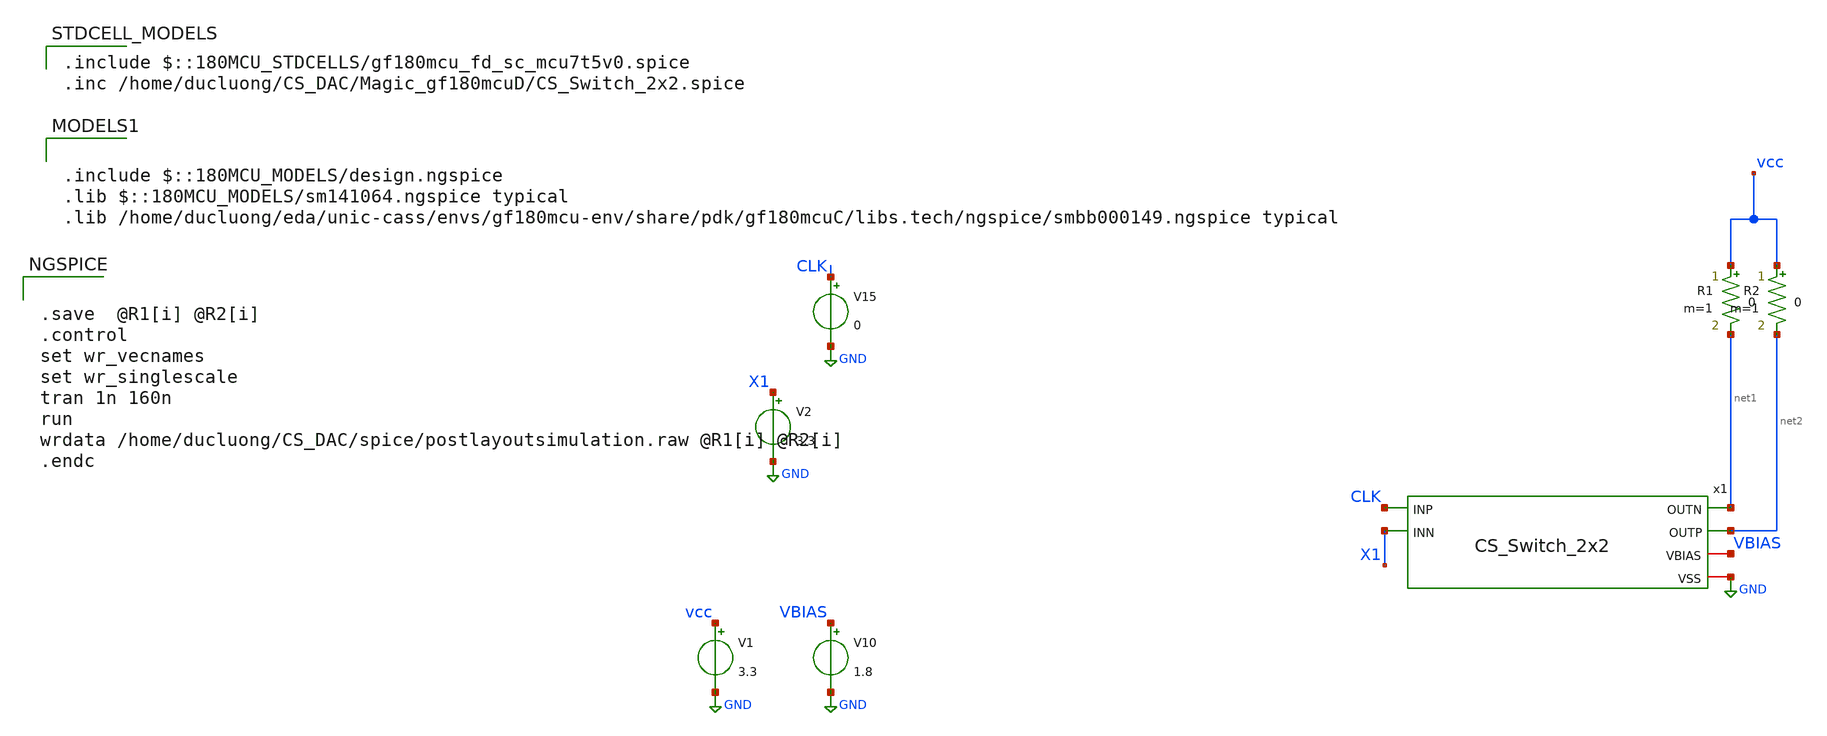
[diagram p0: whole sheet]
** sch_path: xschem/CS1_tb.sch
**.subckt CS1_tb
V2 X1 GND 3.3
V15 CLK GND 0
V1 vcc GND 3.3
V10 VBIAS GND 1.8
R1 vcc net1 0 m=1
R2 vcc net2 0 m=1
x1 CLK X1 net2 net1 VBIAS GND CS_Switch_2x2
**** begin user architecture code

.include $::180MCU_MODELS/design.ngspice
.lib $::180MCU_MODELS/sm141064.ngspice typical
.lib /home/ducluong/eda/unic-cass/envs/gf180mcu-env/share/pdk/gf180mcuC/libs.tech/ngspice/smbb000149.ngspice typical

 .include $::180MCU_STDCELLS/gf180mcu_fd_sc_mcu7t5v0.spice
.inc /home/ducluong/CS_DAC/Magic_gf180mcuD/CS_Switch_2x2.spice


.save  @R1[i] @R2[i]
.control
set wr_vecnames
set wr_singlescale
tran 1n 160n
run
wrdata /home/ducluong/CS_DAC/spice/postlayoutsimulation.raw @R1[i] @R2[i]
.endc


**** end user architecture code
**.ends
.GLOBAL GND
.end
